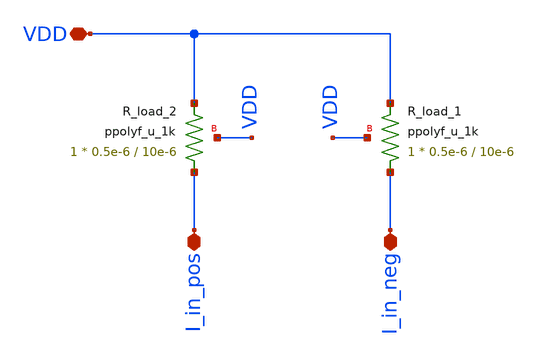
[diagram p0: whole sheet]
** sch_path: src/design_xsch/Gilbert_cell_hierarchal_loading_stage.sch
**.subckt Gilbert_cell_hierarchal_loading_stage I_in_neg I_in_pos VDD
*.iopin I_in_neg
*.iopin I_in_pos
*.iopin VDD
XR_load_2 I_in_pos VDD VDD ppolyf_u_1k r_width=0.5e-6 r_length=10e-6 m=1
XR_load_1 I_in_neg VDD VDD ppolyf_u_1k r_width=0.5e-6 r_length=10e-6 m=1
**.ends
.end
